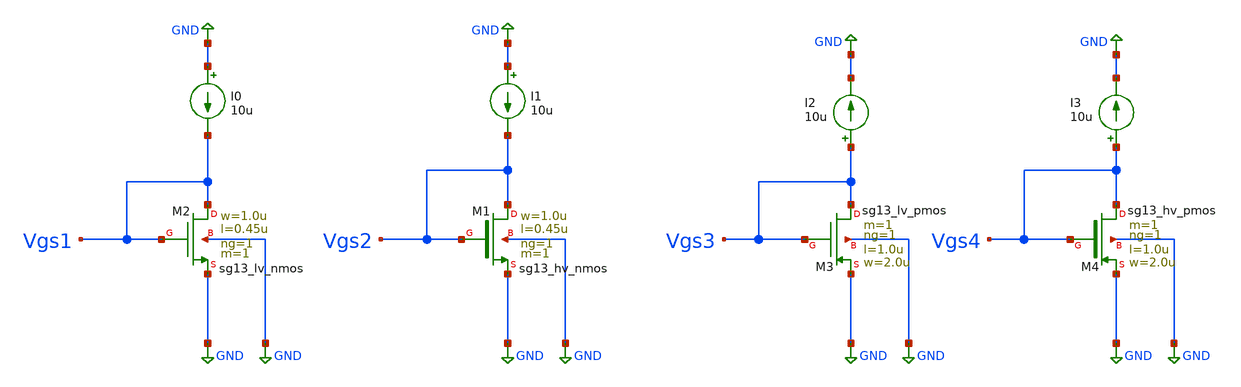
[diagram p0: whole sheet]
** sch_path: ihp-sg13g2/xschem_libs/sg13g2_tests_ase/dc_mos_cs_temp/schematic/dc_mos_cs_temp.sch
* Copyright 2023 IHP PDK Authors
**.subckt dc_mos_cs_temp
XM3 Vgs3 Vgs3 GND GND sg13_lv_pmos w=2.0u l=1.0u ng=1 m=1 mm_ok=1
XM4 Vgs4 Vgs4 GND GND sg13_hv_pmos w=2.0u l=1.0u ng=1 m=1 mm_ok=1
I0 GND Vgs1 10u
I1 GND Vgs2 10u
I2 Vgs3 GND 10u
I3 Vgs4 GND 10u
XM1 Vgs2 Vgs2 GND GND sg13_hv_nmos w=1.0u l=0.45u ng=1 m=1 mm_ok=1
XM2 Vgs1 Vgs1 GND GND sg13_lv_nmos w=1.0u l=0.45u ng=1 m=1 mm_ok=1
**.ends
.GLOBAL GND
.end
